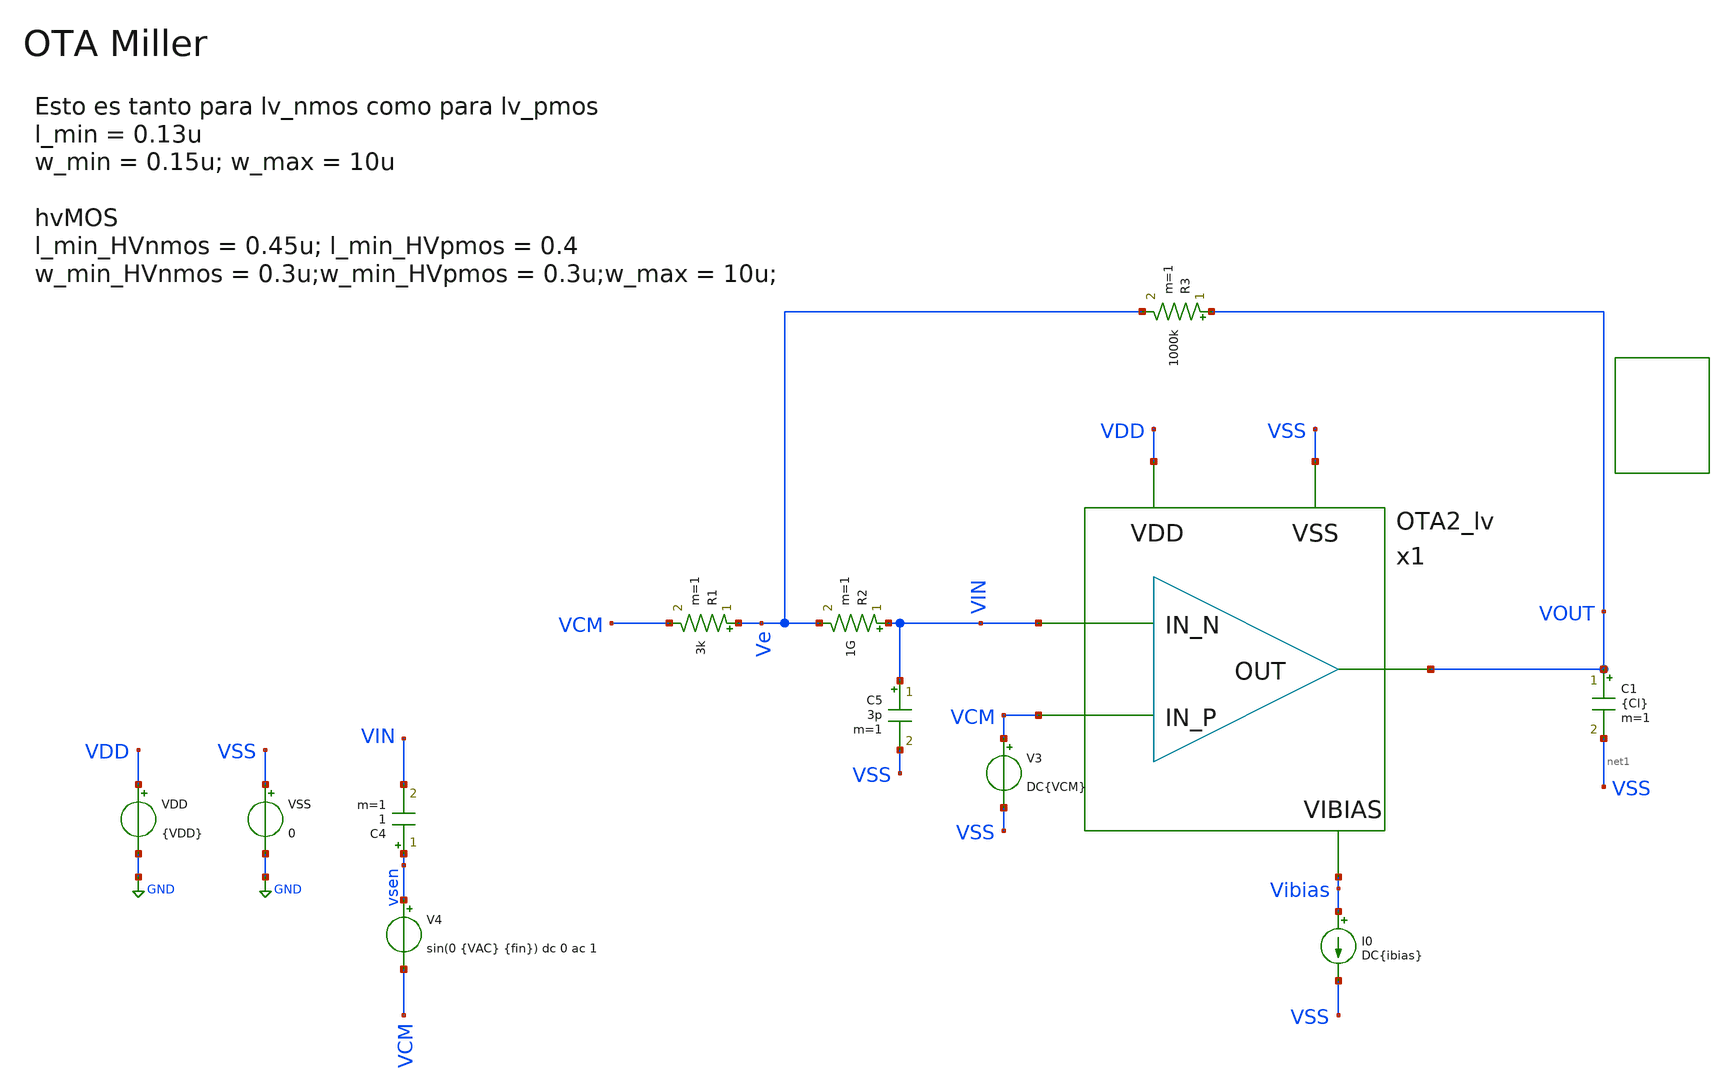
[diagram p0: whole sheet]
** sch_path: xschem/Tareas/Tarea_2/TB_OTA2_OL.sch
**.subckt TB_OTA2_OL
VDD VDD GND {VDD}
I0 Vibias VSS DC{ibias}
R3 VOUT Ve 1000k m=1
V3 VCM VSS DC{VCM}
VSS VSS GND 0
C5 VIN VSS 3p m=1
R2 VIN Ve 1G m=1
R1 Ve VCM 3k m=1
C1 VOUT net1 {Cl} m=1
V4 vsen VCM sin(0 {VAC} {fin}) dc 0 ac 1
C4 vsen VIN 1 m=1
x1 VIN VCM VOUT VDD VSS Vibias OTA2_lv
**** begin user architecture code


*.param VDD = 3.3
.param Ibias = 100u
.param Pi = 3.14159265

.param VAC  = 10m
.param fin  = 9.765625e5

*.ic v(Vo) = 0

* OP Parameters & Singals to save
.save all

*.option temp = 125
*.option temp = -40
.option temp = 27





.lib cornerMOShv.lib mos_tt
.lib cornerMOSlv.lib mos_tt
*.lib cornerMOShv.lib mos_ff
*.lib cornerMOSlv.lib mos_ff
*.lib cornerMOShv.lib mos_ss
*.lib cornerMOSlv.lib mos_ss
*.lib cornerMOShv.lib mos_sf
*.lib cornerMOSlv.lib mos_sf
*.lib cornerMOShv.lib mos_fs
*.lib cornerMOSlv.lib mos_fs

.include /opt/pdks/ihp-sg13g2/libs.ref/sg13g2_stdcell/spice/sg13g2_stdcell.spice
.lib $::SG13G2_MODELS/cornerRES.lib res_typ
.lib $::SG13G2_MODELS/cornerCAP.lib cap_typ
*.lib $::SG13G2_MODELS/diodes.lib




.control
  set color0 = white
  *IPD413
 ac dec 200 1 1000Meg
 settype decibel VOUT
 *setplot ac1

 let phase_val = (180/PI)*cph(VOUT)
 let phase_margin_val = 180 + 180/PI*cph(VOUT)
 settype phase phase_val
 *meas ac PM find phase_margin_val when vdb(VOUT)=0
 meas ac PM find phase_val when vdb(VOUT)=0
 meas ac GM find vdb(vout) when vp(vout)=0
 *meas ac GM2 find vdb(vout) when vp(vout)=-180
 meas ac GBW WHEN vdb(VOUT)=0
 meas ac DCG find vdb(vout) at=1
 let DCG_BW = {DCG} - 3
 meas ac BW WHEN vdb(VOUT)={DCG_BW}

 let Av = 10^(DCG/20)
 print Av

 plot vdb(VOUT)
 plot phase_val
 plot phase_val vdb(VOUT)


 *wrdata /foss/designs/IPD413_2023_HW3_git/Data/data_phaseOTA1.dat phase_val
 *wrdata /foss/designs/IPD413_2023_HW3_git/Data/data_VdbOTA1.dat vdb(out)

 reset
  *DACI
  *ac dec 100 1 10G
  *setplot ac1
  *meas ac GBW when vdb(vout)=0
  *meas ac DCG find vdb(vout) at=1
  *meas ac PM find vp(vout) when vdb(vout)=0
  *print PM*180/PI
  *meas ac GM find vdb(vout) when vp(vout)=0

  *plot vdb(vout)
  *plot {vp(vout)*180/PI}
  *plot vdb(vout) {vp(vout)*180/PI}
.endc


.end





.param VDD = 1.2
.param VCM = 0.6

.control
reset
  op
  setplot op1
  unset filetype
  * VM1
  let VsdM1 = v(x1.VA) - v(x1.VB)
  let VsgM1 = v(x1.VA) - v(VCM)
  let VthM1 = @n.x1.xm1.nsg13_lv_pmos[vth]
  let VovM1 = VsgM1 - VthM1
  let gmM1 = @n.x1.xm1.nsg13_lv_pmos[gm]
  let gdsM1 = @n.x1.xm1.nsg13_lv_pmos[gds]
  let RoM1 = 1/gdsM1
  let CggM1 = @n.x1.xm1.nsg13_lv_pmos[cgg]
  * VM2
  let VsdM2 = v(x1.VA) - v(x1.VC)
  let VsgM2 = v(x1.VA) - v(VIN)
  let VthM2 = @n.x1.xm2.nsg13_lv_pmos[vth]
  let VovM2 = VsgM2 - VthM2
  let gmM2 = @n.x1.xm2.nsg13_lv_pmos[gm]
  let IdM2 = @n.x1.xm2.nsg13_lv_pmos[ids]
  let gdsM2 = @n.x1.xm2.nsg13_lv_pmos[gds]
  let RoM2 = 1/gdsM2
  let gmIdM2 = gmM2/IdM2
  * VM3
  let VdsM3 = v(x1.VB) - v(VSS)
  let VthM3 = @n.x1.xm3.nsg13_lv_nmos[vth]
  let gmM3 = @n.x1.xm3.nsg13_lv_nmos[gm]
  let gdsM3 = @n.x1.xm3.nsg13_lv_nmos[gds]
  let RoM3 = 1/gdsM3
  * VM4
  let VdsM4 = v(x1.VC) - v(VSS)
  let VgsM4 = v(x1.VB) - v(VSS)
  let VthM4 = @n.x1.xm4.nsg13_lv_nmos[vth]
  let VovM4 = VgsM4 - VthM4
  let gmM4 = @n.x1.xm4.nsg13_lv_nmos[gm]
  let gdsM4 = @n.x1.xm4.nsg13_lv_nmos[gds]
  let RoM4 = 1/gdsM4
  * VM5

  let VsdM5 = v(VDD) - v(x1.VA)
  let VsgM5 = v(VDD) - v(Vibias)
  let VthM5 = @n.x1.xm5.nsg13_lv_pmos[vth]
  let VovM5 = VsgM5 - VthM5
  let gmM5 = @n.x1.xm5.nsg13_lv_pmos[gm]
  let gdsM5 = @n.x1.xm5.nsg13_lv_pmos[gds]
  let RoM5 = 1/gdsM5
  * VM6
  let VdsM6 = v(VOUT) - v(VSS)
  let VgsM6 = v(x1.VC) - v(VSS)
  let VthM6 = @n.x1.xm6.nsg13_lv_nmos[vth]
  let VovM6 = VgsM6 - VthM6
  let gmM6 = @n.x1.xm6.nsg13_lv_nmos[gm]
  let IdM6 = @n.x1.xm6.nsg13_lv_nmos[ids]
  let gdsM6 = @n.x1.xm6.nsg13_lv_nmos[gds]
  let CggM6 = @n.x1.xm6.nsg13_lv_nmos[cgg]
  let RoM6 = 1/gdsM6
  let gmIdM6 = gmM6/IdM6
  * VM7
  let VsdM7 = v(VDD) - v(VOUT)
  let VsgM7 = v(VDD) - v(Vibias)
  let VthM7 = @n.x1.xm7.nsg13_lv_pmos[vth]
  let VovM7 = VsgM7 - VthM7
  let gmM7 = @n.x1.xm7.nsg13_lv_pmos[gm]
  let gdsM7 = @n.x1.xm7.nsg13_lv_pmos[gds]
  let RoM7 = 1/gdsM7
  * VM8
  let VsdM8 = v(VDD) - v(Vibias)
  let VthM8 = @n.x1.xm8.nsg13_lv_pmos[vth]
  let VovM8 = VsdM8 - VthM8
  let gmM8 = @n.x1.xm8.nsg13_lv_pmos[gm]
  let gdsM8 = @n.x1.xm8.nsg13_lv_pmos[gds]
  let RoM8 = 1/gdsM8
  * VMR
  let VdsMR = v(x1.VC) - v(x1.VsMR)
  let gdsMR = @n.x1.xm9.nsg13_lv_nmos[gds]
  let RoMR = 1/gdsMR

  let Ro24 = 1/(gdsM2+gdsM4)
  let Ro67 = 1/(gdsM7+gdsM6)
  let Av1 = gmM1/(gdsM2+gdsM4)
  let Av2 = gmM6/(gdsM7+gdsM6)
  let Av = Av1*Av2
  let BW = (gdsM2+gdsM4)/(2*pi*Av2*{Cc})
  let gdsM2_gdsM4 = gdsM2+gdsM4
  let w22 = gmM6/((CggM6+{Cl}))
  *let w2 = gmM6/(({Cl})*(1+CggM6/{Cc}))
  *let w2 = gmM6/(2*pi*{Cl}*(1+CggM6/{Cc}))
  let w2 = gmM6/({Cl}*(1+CggM6/{Cc}))
  let cggM6_cc = CggM6/{Cc}
  let GBW = gmM1/(2*pi*{Cc})
  *let GBW2 = gmM1/{Cc}
  let DCG = 20*log10(Av)
  *let fnd = gmM6/(2*pi*{Cl})

  let Cc_eq = gmM2/{GBW_Objetivo}
  let Cc = {Cc}
  let gm12_Objetivo = {GBW_Objetivo}*{Cc}
  let idm12_Objetivo = gm12_Objetivo/10
  *let gm6_Objetivo = 3*{GBW_Objetivo}*{Cl}
  *let gm6_Objetivo = 3*{GBW_Objetivo}*({Cl}*(1+CggM6/{Cc}))
  *let gm6_Objetivo = 3*{GBW_Objetivo}*({Cl}*(1+CggM6/{Cc}))/(2*pi)
   let gm6_Objetivo = 3*{GBW_Objetivo}*(CggM6+{Cl})/(2*pi)
   let idm6_Objetivo = gm6_Objetivo/10

  print Av1 Av2 Av DCG
  print BW GBW w2
  print Cc
  print w2 w22


  write TB_OTA2_OL.raw
.endc

.end




.param temp=27

.param m_M8 = 1
.param m_M7 = 1
.param m_M5 = 1
.param w_M8 =0.15u
.param w_M7 =0.15u
.param w_M5 =0.15u
.param l_M875 = 0.13u

.param m_M12 = 1
.param w_M12 =0.15u
.param l_M12 = 0.13u

.param m_M34 = 1
.param w_M34 =0.15u
.param l_M34 = 0.13u

.param m_M6 = 1
.param w_M6 =0.15u
.param l_M6 = 0.13u

.param Cc = 0.1p
.param Cl = 5p
.csparam Cl = {Cl}
.csparam Cc = {Cc}

* Requisitos de diseño
.param Cl = 5p
.csparam Cl = {Cl}
.param GBW_Objetivo= 2*Pi*100Meg
.csparam GBW_Objetivo = {GBW_Objetivo}

.param Cc = Cl*0.01
.csparam Cc = {Cc}






**** end user architecture code
**.ends

* expanding   symbol:  ../Tarea_2/OTA2_lv.sym # of pins=6
** sym_path: ../Tarea_2/OTA2_lv.sym
** sch_path: ../Tarea_2/OTA2_lv.sch
.subckt OTA2_lv IN_N IN_P OUT VDD VSS Vibias
*.ipin IN_N
*.ipin IN_P
*.ipin Vibias
*.opin OUT
*.iopin VDD
*.iopin VSS
XM1 VB IN_N net1 VA sg13_lv_pmos w={w_M12} l={l_M12} ng=1 m={m_M12} mm_ok=1
XM3 VSS VB VB VSS sg13_lv_nmos w={w_M34} l={l_M34} ng=1 m={m_M34} mm_ok=1
XM2 VC IN_P net2 VA sg13_lv_pmos w={w_M12} l={l_M12} ng=1 m={m_M12} mm_ok=1
XM4 VSS VB net6 VSS sg13_lv_nmos w={w_M34} l={l_M34} ng=1 m={m_M34} mm_ok=1
XM5 net7 Vibias VDD VDD sg13_lv_pmos w={w_M5} l={l_M875} ng=1 m={m_M5} mm_ok=1
XM6 VSS VC net3 VSS sg13_lv_nmos w={w_M6} l={l_M6} ng=1 m={m_M6} mm_ok=1
XM7 net5 Vibias VDD VDD sg13_lv_pmos w={w_M7} l={l_M875} ng=1 m={m_M7} mm_ok=1
XM8 net8 Vibias VDD VDD sg13_lv_pmos w={w_M8} l={l_M875} ng=1 m={m_M8} mm_ok=1
C1 VC net4 {Cc} m=1
Vmeas VA net1 0
.save i(vmeas)
Vmeas1 VC net6 0
.save i(vmeas1)
Vmeas2 VA net2 0
.save i(vmeas2)
Vmeas3 net4 net3 0
.save i(vmeas3)
Vmeas4 net5 net4 0
.save i(vmeas4)
Vmeas5 net7 VA 0
.save i(vmeas5)
Vmeas6 net8 Vibias 0
.save i(vmeas6)
Vmeas7 net4 OUT 0
.save i(vmeas7)
.ends

.GLOBAL GND
.end
